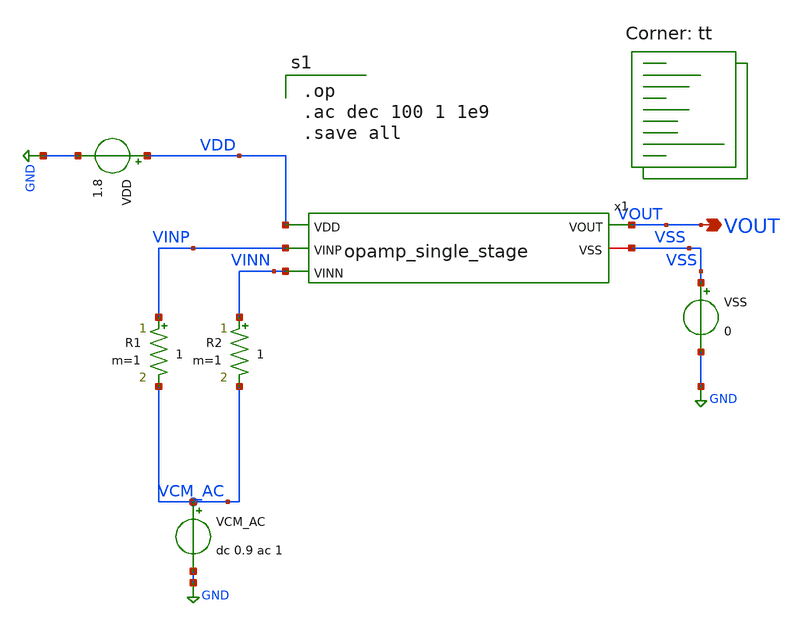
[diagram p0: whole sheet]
** sch_path: schematics/tb_cmrr.sch
**.subckt tb_cmrr VOUT
*.opin VOUT
VDD VDD GND 1.8
VCM_AC VCM_AC GND dc 0.9 ac 1
VSS VSS GND 0
x1 VDD VOUT VINP VINN VSS opamp_single_stage
R1 VINP VCM_AC 1 m=1
R2 VINN VCM_AC 1 m=1
**** begin user architecture code

.op
.ac dec 100 1 1e9
.save all


.lib $::SKYWATER_MODELS/sky130.lib.spice tt
**** end user architecture code
**.ends
.GLOBAL GND
.end
